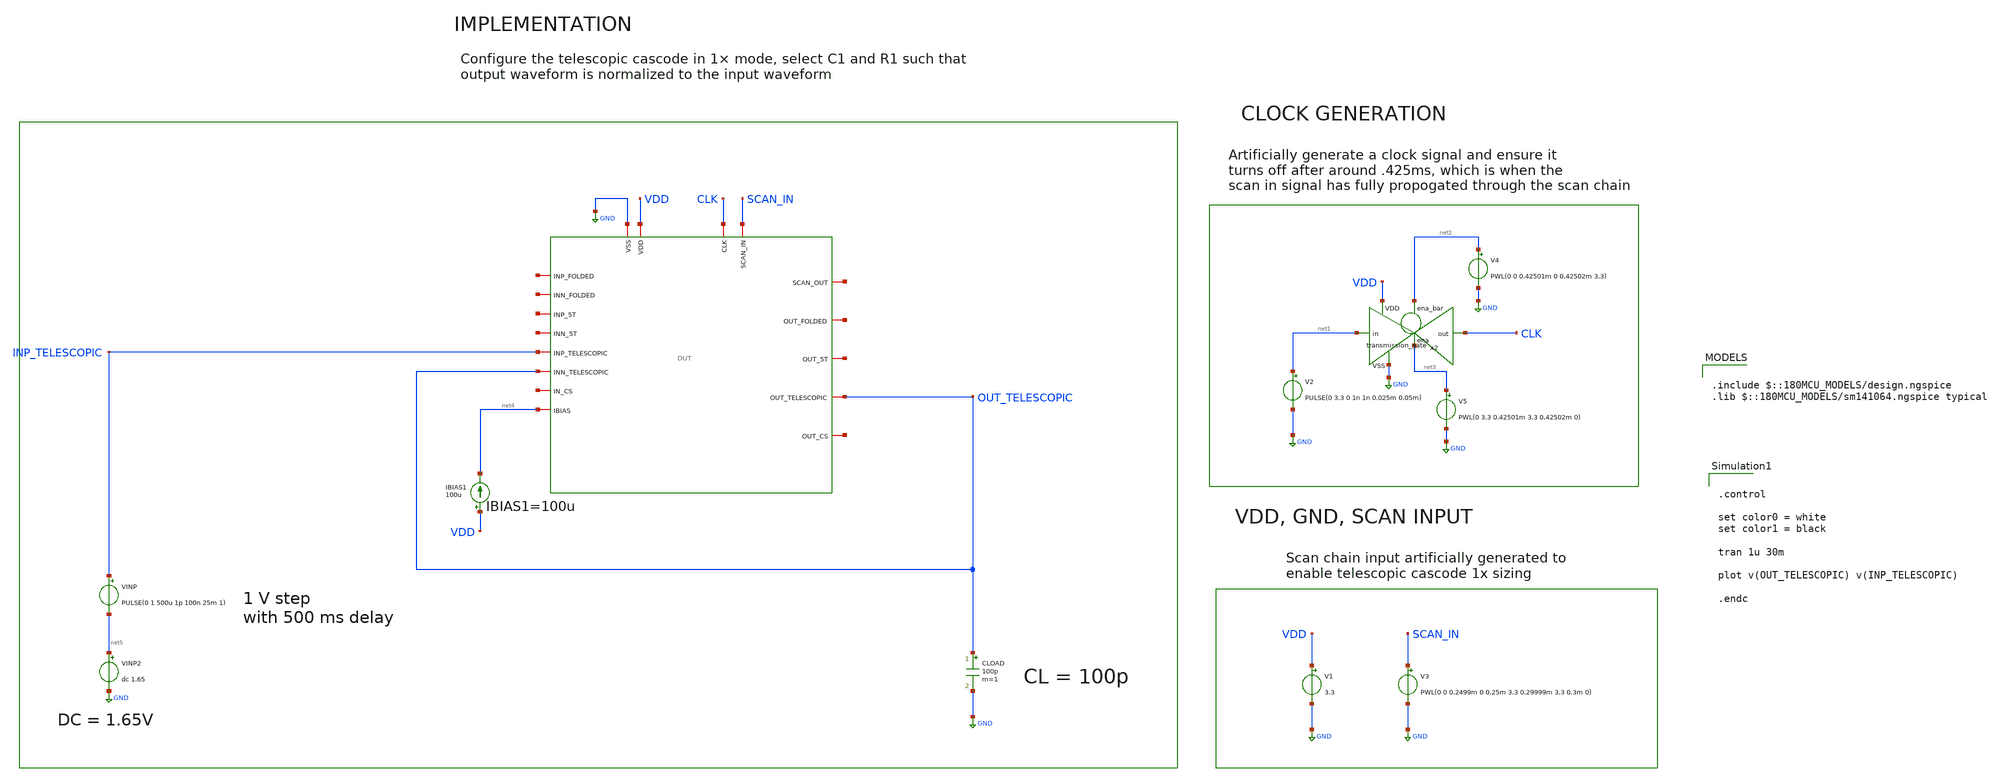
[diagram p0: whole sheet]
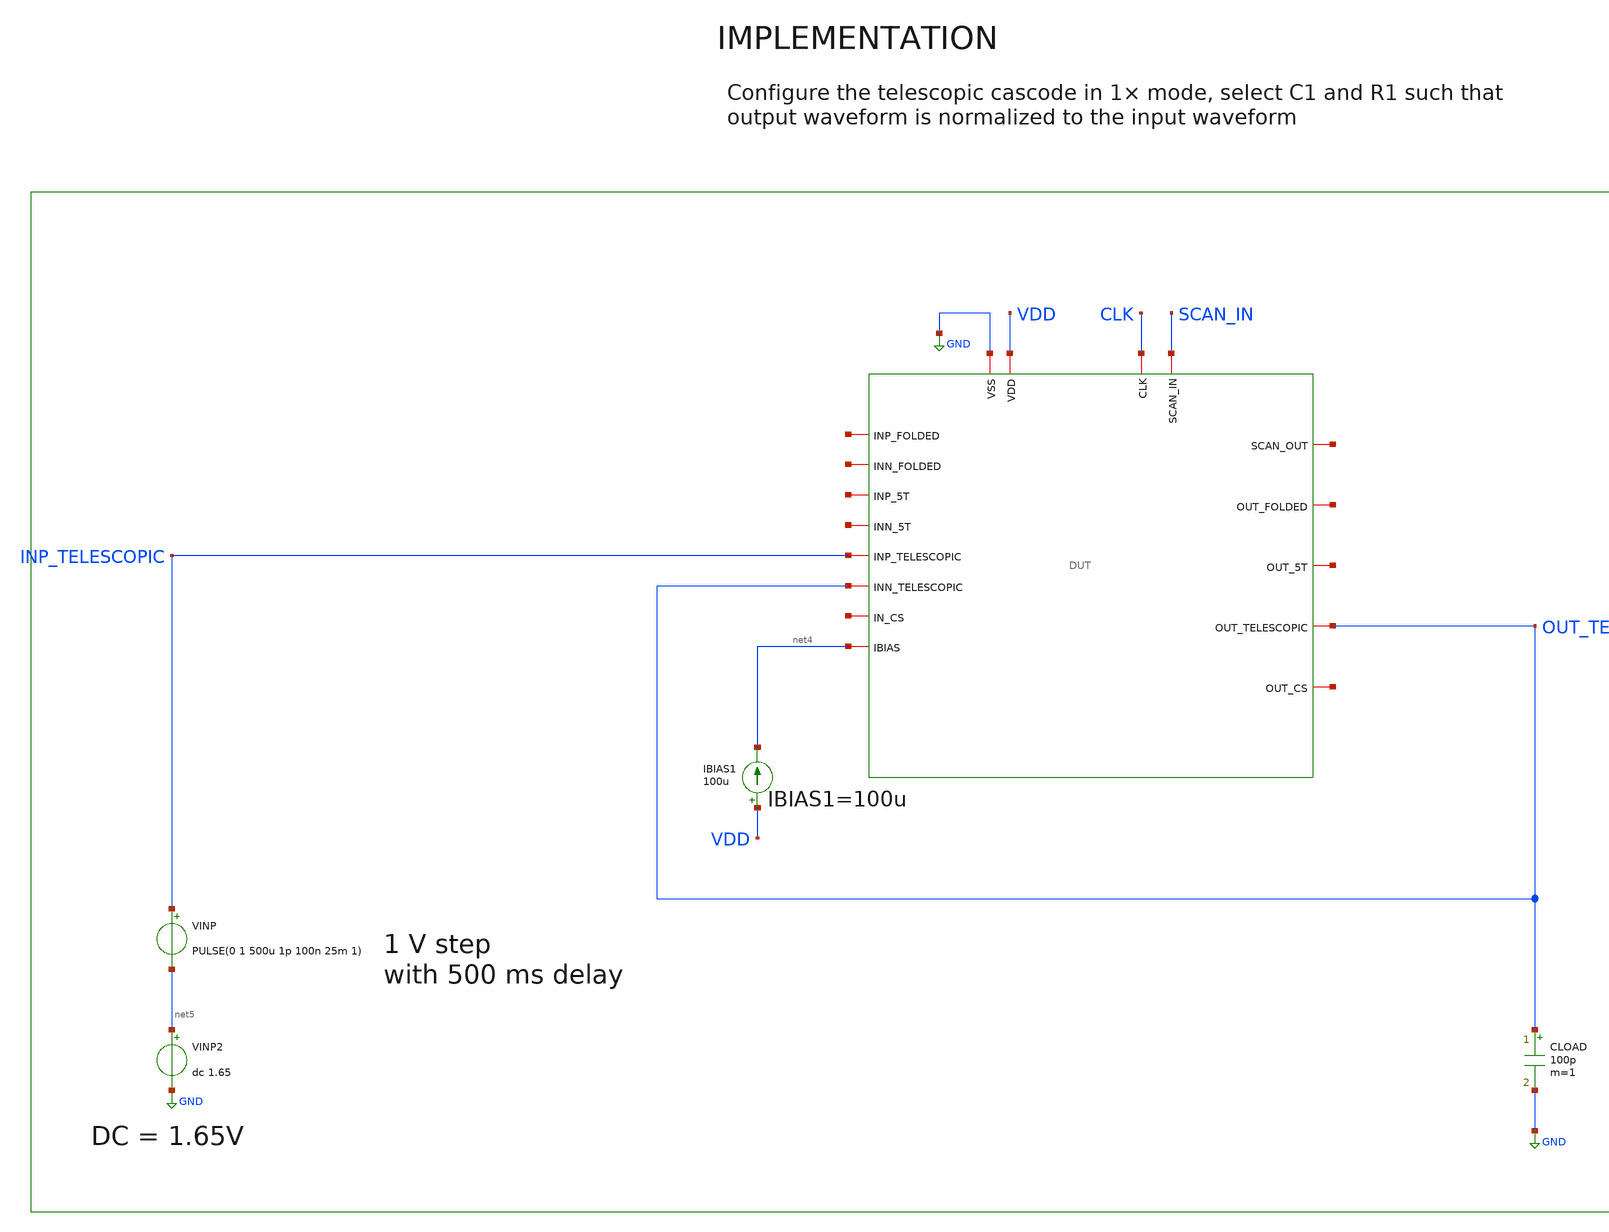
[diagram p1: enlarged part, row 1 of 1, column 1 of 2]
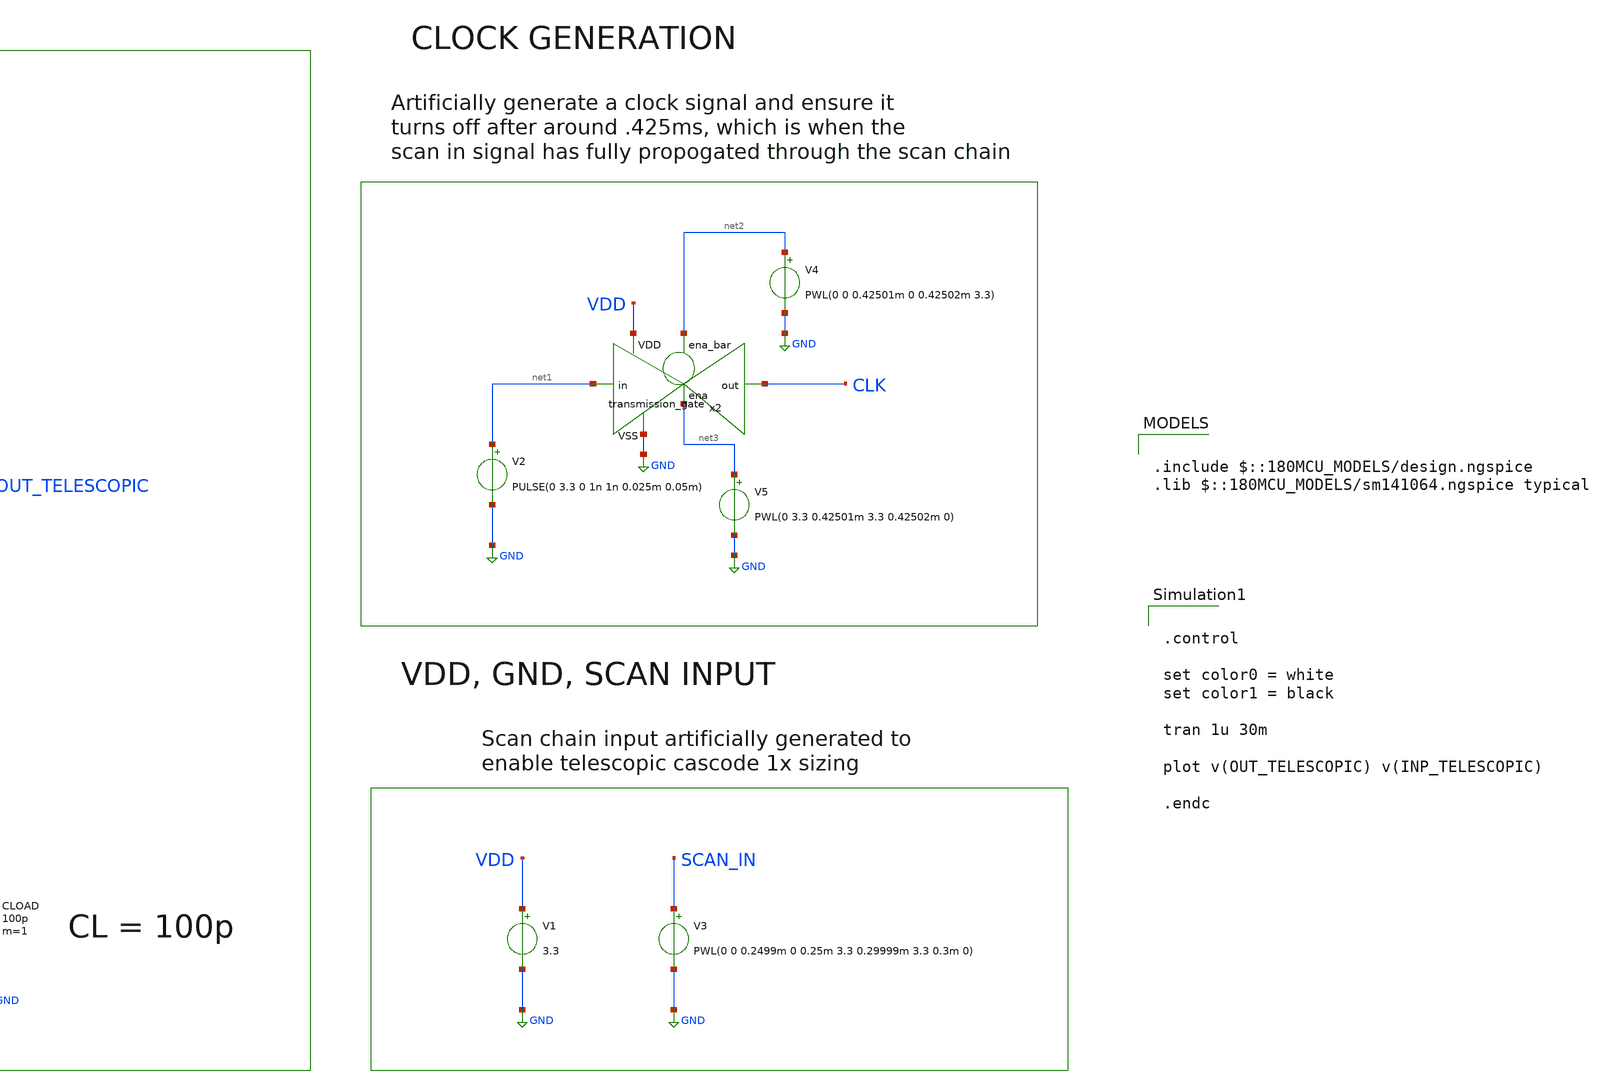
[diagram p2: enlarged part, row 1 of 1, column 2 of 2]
** sch_path: designs/libs/core_tb/mpg/Unity_Step.sch
**.subckt Unity_Step
V3 SCAN_IN GND PWL(0 0 0.2499m 0 0.25m 3.3 0.29999m 3.3 0.3m 0)
V1 VDD GND 3.3
V2 net1 GND PULSE(0 3.3 0 1n 1n 0.025m 0.05m)
x2 net2 VDD CLK net1 GND net3 transmission_gate
V4 net2 GND PWL(0 0 0.42501m 0 0.42502m 3.3)
V5 net3 GND PWL(0 3.3 0.42501m 3.3 0.42502m 0)
IBIAS1 VDD net4 100u
CLOAD OUT_TELESCOPIC GND 100p m=1
x1 CLK net6 SCAN_IN GND VDD net7 net8 net9 net4 net10 net11 net12 INP_TELESCOPIC OUT_TELESCOPIC
+ net13 net14 OUT_TELESCOPIC DUT
VINP2 net5 GND dc 1.65
VINP INP_TELESCOPIC net5 PULSE(0 1 500u 1p 100n 25m 1)
**** begin user architecture code

.include $::180MCU_MODELS/design.ngspice
.lib $::180MCU_MODELS/sm141064.ngspice typical



.control

set color0 = white
set color1 = black

tran 1u 30m

plot v(OUT_TELESCOPIC) v(INP_TELESCOPIC)

.endc

**** end user architecture code
**.ends
.GLOBAL GND
.end
